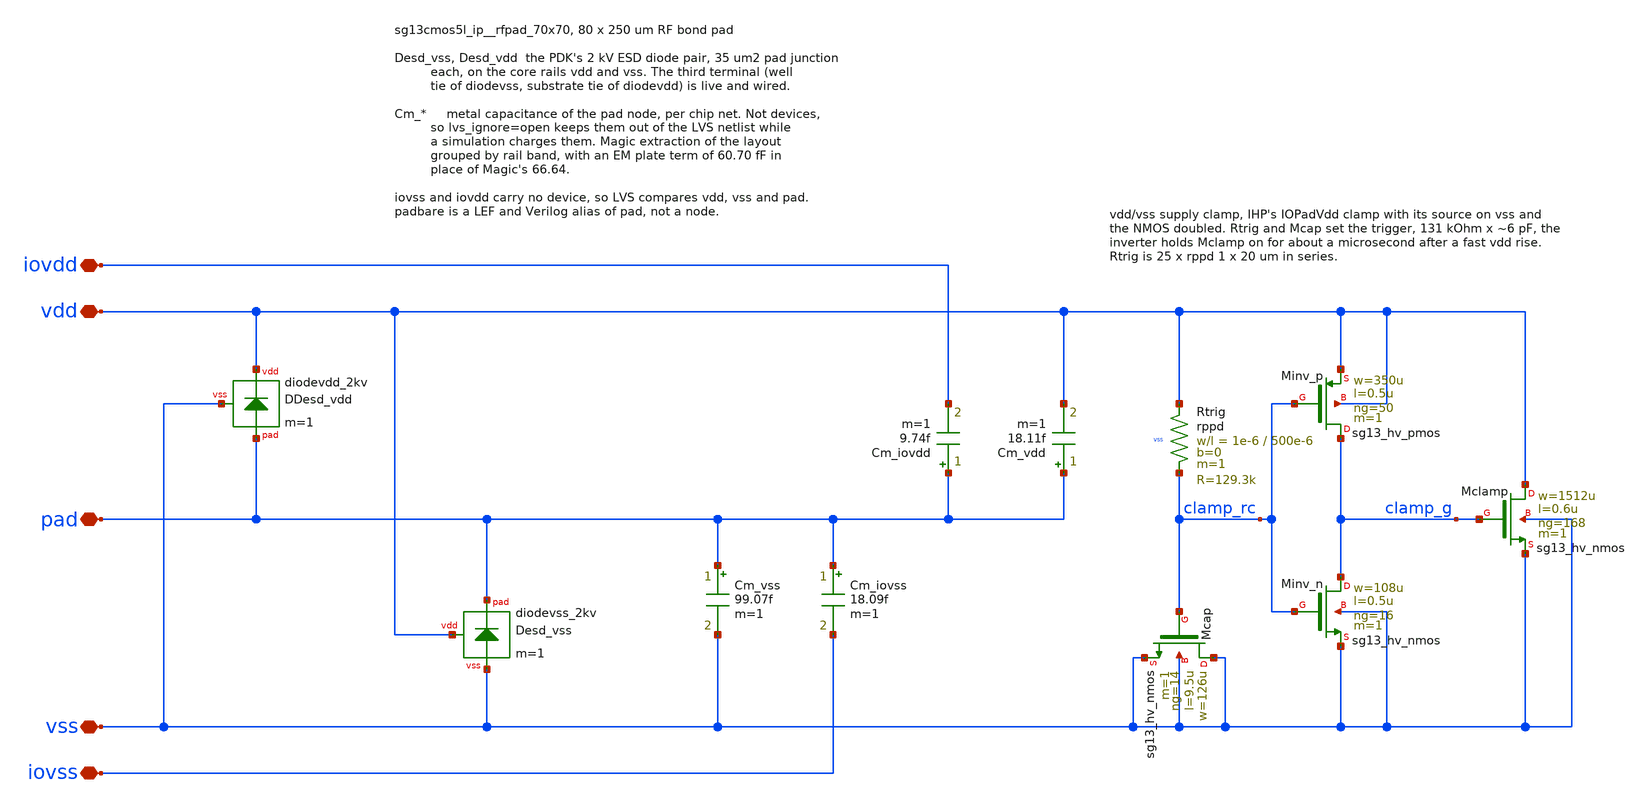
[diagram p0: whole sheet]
** sch_path: ip/sg13cmos5l_ip__bondpad_70x70/schematic/xschem/sg13cmos5l_ip__rfpad_70x70.sch
* (c) 2026 Harald Pretl, JKU, Apache-2.0 WITH SHL-2.1
**.subckt sg13cmos5l_ip__rfpad_70x70 vss vdd iovss iovdd pad
*.iopin vss
*.iopin vdd
*.iopin iovss
*.iopin iovdd
*.iopin pad
XDesd_vdd vdd pad vss diodevdd_2kv m=1
XDesd_vss vdd pad vss diodevss_2kv m=1
Cm_vss pad vss 99.07f m=1
Cm_iovss pad iovss 18.09f m=1
Cm_iovdd pad iovdd 9.74f m=1
Cm_vdd pad vdd 18.11f m=1
XMclamp vdd clamp_g vss vss sg13_hv_nmos w=1512u l=0.6u ng=168 m=1 mm_ok=1
XMcap vss clamp_rc vss vss sg13_hv_nmos w=126u l=9.5u ng=14 m=1 mm_ok=1
XMinv_n clamp_g clamp_rc vss vss sg13_hv_nmos w=108u l=0.5u ng=16 m=1 mm_ok=1
XMinv_p clamp_g clamp_rc vdd vdd sg13_hv_pmos w=350u l=0.5u ng=50 m=1 mm_ok=1
XRtrig vdd clamp_rc vss rppd w=1e-6 l=500e-6 m=1 b=0 mm_ok=1
**.ends
.end
